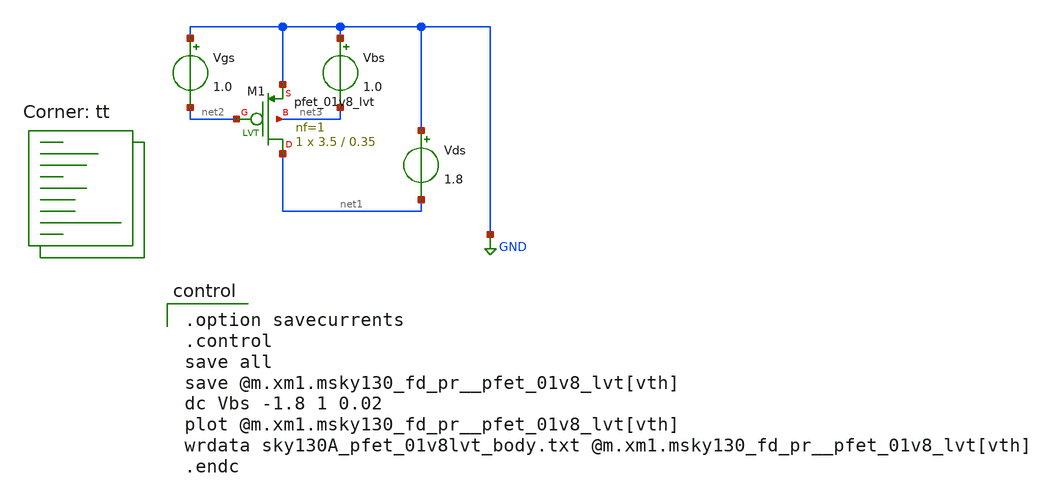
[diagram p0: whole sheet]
** sch_path: xschem/MOSFET/sky130A_pfet_01v8lvt_body.sch
**.subckt sky130A_pfet_01v8lvt_body
Vgs GND net2 1.0
Vds GND net1 1.8
Vbs GND net3 1.0
XM1 net1 net2 GND net3 sky130_fd_pr__pfet_01v8_lvt L=0.35 W=3.5 nf=1 ad='int((1 + 1)/2) * 3.5 / 1 * 0.29'
+ as='int((1 + 2)/2) * 3.5 / 1 * 0.29' pd='2*int((1 + 1)/2) * (3.5 / 1 + 0.29)' ps='2*int((1 + 2)/2) * (3.5 / 1 + 0.29)'
+ nrd='0.29 / 3.5 ' nrs='0.29 / 3.5 ' sa=0 sb=0 sd=0 mult=1 m=1
**** begin user architecture code

.option savecurrents
.control
save all
save @m.xm1.msky130_fd_pr__pfet_01v8_lvt[vth]
dc Vbs -1.8 1 0.02
plot @m.xm1.msky130_fd_pr__pfet_01v8_lvt[vth]
wrdata sky130A_pfet_01v8lvt_body.txt @m.xm1.msky130_fd_pr__pfet_01v8_lvt[vth]
.endc

.lib $::SKYWATER_MODELS/sky130.lib.spice tt
**** end user architecture code
**.ends
.GLOBAL GND
.end
